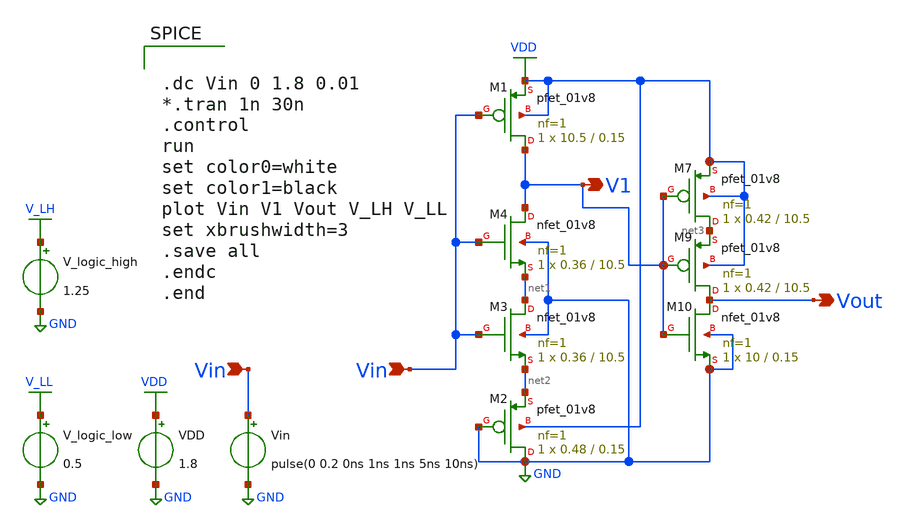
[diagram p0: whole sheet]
** sch_path: xschem/Vth_sch/th15_test.sch
**.subckt th15_test Vin Vin V1 Vout
*.ipin Vin
*.ipin Vin
*.opin V1
*.opin Vout
VDD VDD GND 1.8
Vin Vin GND pulse(0 0.2 0ns 1ns 1ns 5ns 10ns)
XM1 V1 Vin VDD VDD sky130_fd_pr__pfet_01v8 L=0.15 W=10.5 nf=1 ad='int((nf+1)/2) * W/nf * 0.29' as='int((nf+2)/2) * W/nf * 0.29'
+ pd='2*int((nf+1)/2) * (W/nf + 0.29)' ps='2*int((nf+2)/2) * (W/nf + 0.29)' nrd='0.29 / W' nrs='0.29 / W'
+ sa=0 sb=0 sd=0 mult=1 m=1
V_logic_high V_LH GND 1.25
V_logic_low V_LL GND 0.5
XM3 net1 Vin net2 GND sky130_fd_pr__nfet_01v8 L=10.5 W=0.36 nf=1 ad='int((nf+1)/2) * W/nf * 0.29' as='int((nf+2)/2) * W/nf * 0.29'
+ pd='2*int((nf+1)/2) * (W/nf + 0.29)' ps='2*int((nf+2)/2) * (W/nf + 0.29)' nrd='0.29 / W' nrs='0.29 / W'
+ sa=0 sb=0 sd=0 mult=1 m=1
XM4 V1 Vin net1 GND sky130_fd_pr__nfet_01v8 L=10.5 W=0.36 nf=1 ad='int((nf+1)/2) * W/nf * 0.29' as='int((nf+2)/2) * W/nf * 0.29'
+ pd='2*int((nf+1)/2) * (W/nf + 0.29)' ps='2*int((nf+2)/2) * (W/nf + 0.29)' nrd='0.29 / W' nrs='0.29 / W'
+ sa=0 sb=0 sd=0 mult=1 m=1
XM2 GND GND net2 VDD sky130_fd_pr__pfet_01v8 L=0.15 W=0.48 nf=1 ad='int((nf+1)/2) * W/nf * 0.29' as='int((nf+2)/2) * W/nf * 0.29'
+ pd='2*int((nf+1)/2) * (W/nf + 0.29)' ps='2*int((nf+2)/2) * (W/nf + 0.29)' nrd='0.29 / W' nrs='0.29 / W'
+ sa=0 sb=0 sd=0 mult=1 m=1
XM7 net3 V1 VDD VDD sky130_fd_pr__pfet_01v8 L=10.5 W=0.42 nf=1 ad='int((nf+1)/2) * W/nf * 0.29' as='int((nf+2)/2) * W/nf * 0.29'
+ pd='2*int((nf+1)/2) * (W/nf + 0.29)' ps='2*int((nf+2)/2) * (W/nf + 0.29)' nrd='0.29 / W' nrs='0.29 / W'
+ sa=0 sb=0 sd=0 mult=1 m=1
XM9 Vout V1 net3 VDD sky130_fd_pr__pfet_01v8 L=10.5 W=0.42 nf=1 ad='int((nf+1)/2) * W/nf * 0.29' as='int((nf+2)/2) * W/nf * 0.29'
+ pd='2*int((nf+1)/2) * (W/nf + 0.29)' ps='2*int((nf+2)/2) * (W/nf + 0.29)' nrd='0.29 / W' nrs='0.29 / W'
+ sa=0 sb=0 sd=0 mult=1 m=1
XM10 Vout V1 GND GND sky130_fd_pr__nfet_01v8 L=0.15 W=10 nf=1 ad='int((nf+1)/2) * W/nf * 0.29' as='int((nf+2)/2) * W/nf * 0.29'
+ pd='2*int((nf+1)/2) * (W/nf + 0.29)' ps='2*int((nf+2)/2) * (W/nf + 0.29)' nrd='0.29 / W' nrs='0.29 / W'
+ sa=0 sb=0 sd=0 mult=1 m=1
**** begin user architecture code


.lib /usr/local/share/pdk/sky130A/libs.tech/ngspice/sky130.lib.spice tt

.save all





.dc Vin 0 1.8 0.01
*.tran 1n 30n
.control
run
set color0=white
set color1=black
plot Vin V1 Vout V_LH V_LL
set xbrushwidth=3
.save all
.endc
.end


**** end user architecture code
**.ends
.GLOBAL VDD
.GLOBAL GND
.GLOBAL V_LH
.GLOBAL V_LL
.end
